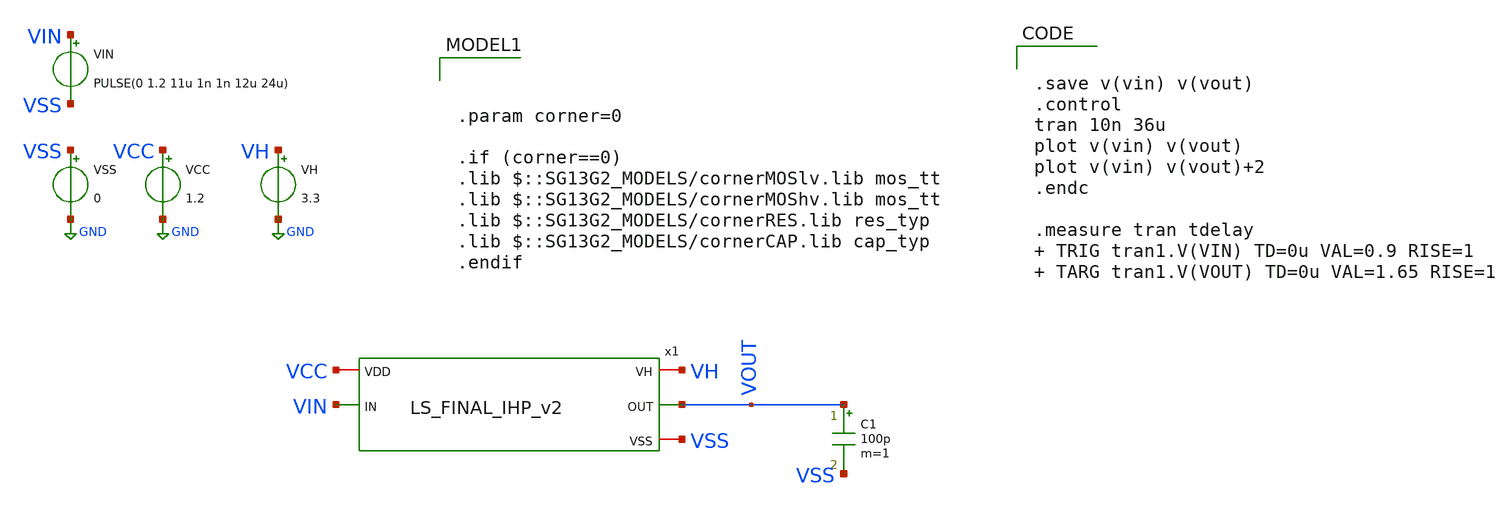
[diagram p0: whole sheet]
** sch_path: xschem/tb_LS_FINAL_IHP_v1p1.sch
**.subckt tb_LS_FINAL_IHP_v1p1
VCC VCC GND 1.2
VSS VSS GND 0
VIN VIN VSS PULSE(0 1.2 11u 1n 1n 12u 24u)
C1 VOUT VSS 100p m=1
x1 VH VCC VIN VOUT VSS LS_FINAL_IHP_v2
VH VH GND 3.3
**** begin user architecture code


.save v(vin) v(vout)
.control
tran 10n 36u
plot v(vin) v(vout)
plot v(vin) v(vout)+2
.endc

.measure tran tdelay  TRIG tran1.V(VIN) TD=0u VAL=0.9 RISE=1  TARG tran1.V(VOUT) TD=0u VAL=1.65
+ RISE=1






.param corner=0

.if (corner==0)
.lib $::SG13G2_MODELS/cornerMOSlv.lib mos_tt
.lib $::SG13G2_MODELS/cornerMOShv.lib mos_tt
.lib $::SG13G2_MODELS/cornerRES.lib res_typ
.lib $::SG13G2_MODELS/cornerCAP.lib cap_typ
.endif

**** end user architecture code
**.ends

* expanding   symbol:  LS_FINAL_IHP_v2.sym # of pins=5
** sym_path: xschem/LS_FINAL_IHP_v2.sym
** sch_path: xschem/LS_FINAL_IHP_v2.sch
.subckt LS_FINAL_IHP_v2 VH VDD IN OUT VSS
*.ipin IN
*.iopin VDD
*.iopin VH
*.opin OUT
*.iopin VSS
XM1 VSS IN net1 VSS sg13_lv_nmos w=1.0u l=0.15u ng=1 m=5 mm_ok=1
XM2 net1 IN VDD VDD sg13_lv_pmos w=1.0u l=0.15u ng=1 m=5 mm_ok=1
XM3 VSS net1 net2 VSS sg13_hv_nmos w=4.0u l=0.5u ng=1 m=3 mm_ok=1
XM4 net2 net3 VH VH sg13_hv_pmos w=2.0u l=0.5u ng=1 m=1 mm_ok=1
XM5 net3 net2 VH VH sg13_hv_pmos w=2.0u l=0.5u ng=1 m=1 mm_ok=1
XM6 VSS IN net3 VSS sg13_hv_nmos w=4.0u l=0.5u ng=1 m=3 mm_ok=1
XM8 net4 net2 VH VH sg13_hv_pmos w=10.0u l=0.5u ng=1 m=10 mm_ok=1
XM9 VSS IN net4 VSS sg13_hv_nmos w=10.0u l=0.5u ng=1 m=10 mm_ok=1
XM7 OUT net4 VH VH sg13_hv_pmos w=10.0u l=0.5u ng=1 m=20 mm_ok=1
XM10 VSS net4 OUT VSS sg13_hv_nmos w=10.0u l=0.5u ng=1 m=20 mm_ok=1
.ends

.GLOBAL GND
.end
